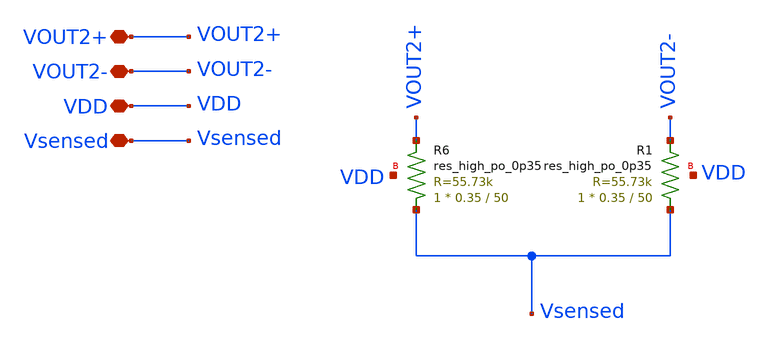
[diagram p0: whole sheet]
** sch_path: old stuff/folded_cascode_amplifier/detector/detector_1.sch
**.subckt detector_1 VOUT2+ VOUT2- VDD Vsensed
*.iopin VOUT2+
*.iopin VOUT2-
*.iopin VDD
*.iopin Vsensed
XR6 Vsensed VOUT2+ VDD sky130_fd_pr__res_high_po_0p35 L=50 mult=1 m=1
XR1 Vsensed VOUT2- VDD sky130_fd_pr__res_high_po_0p35 L=50 mult=1 m=1
**.ends
.end
